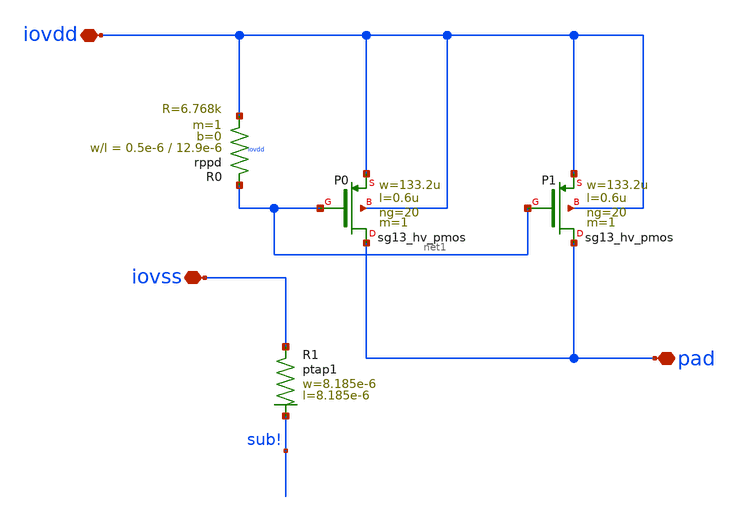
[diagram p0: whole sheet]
** sch_path: ihp-sg13g2/libs.ref/sg13g2_io/sch/xschem/sg13g2_Clamp_P20N0D.sch
**.subckt sg13g2_Clamp_P20N0D iovss pad iovdd
*.iopin iovss
*.iopin pad
*.iopin iovdd
XP0 pad net1 iovdd iovdd sg13_hv_pmos w=133.2u l=0.6u ng=20 m=1 mm_ok=1
XP1 pad net1 iovdd iovdd sg13_hv_pmos w=133.2u l=0.6u ng=20 m=1 mm_ok=1
XR0 net1 iovdd iovdd rppd w=0.5e-6 l=12.9e-6 m=1 b=0 mm_ok=1
XR1 iovss sub! ptap1 R=9.826 w=8.185e-6 l=8.185e-6
**.ends
.end
